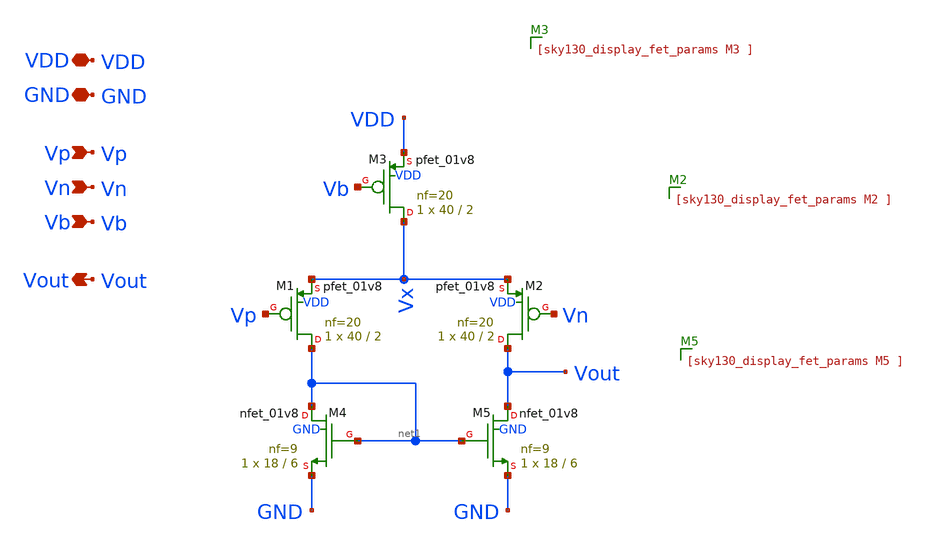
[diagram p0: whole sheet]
** sch_path: sch/archive/old/5t_ota_p.sch
**.subckt 5t_ota_p VDD Vp Vout GND Vn Vb
*.iopin VDD
*.ipin Vp
*.opin Vout
*.iopin GND
*.ipin Vn
*.ipin Vb
XM1 net1 Vp Vx VDD sky130_fd_pr__pfet_01v8 L=2 W=40 nf=20 ad='int((20 + 1)/2) * 40 / 20 * 0.29' as='int((20 + 2)/2) * 40 / 20 * 0.29'
+ pd='2*int((20 + 1)/2) * (40 / 20 + 0.29)' ps='2*int((20 + 2)/2) * (40 / 20 + 0.29)' nrd='0.29 / 40 '
+ nrs='0.29 / 40 ' sa=0 sb=0 sd=0 mult=1 m=1
XM2 Vout Vn Vx VDD sky130_fd_pr__pfet_01v8 L=2 W=40 nf=20 ad='int((20 + 1)/2) * 40 / 20 * 0.29' as='int((20 + 2)/2) * 40 / 20 * 0.29'
+ pd='2*int((20 + 1)/2) * (40 / 20 + 0.29)' ps='2*int((20 + 2)/2) * (40 / 20 + 0.29)' nrd='0.29 / 40 '
+ nrs='0.29 / 40 ' sa=0 sb=0 sd=0 mult=1 m=1
XM3 Vx Vb VDD VDD sky130_fd_pr__pfet_01v8 L=2 W=40 nf=20 ad='int((20 + 1)/2) * 40 / 20 * 0.29' as='int((20 + 2)/2) * 40 / 20 * 0.29'
+ pd='2*int((20 + 1)/2) * (40 / 20 + 0.29)' ps='2*int((20 + 2)/2) * (40 / 20 + 0.29)' nrd='0.29 / 40 '
+ nrs='0.29 / 40 ' sa=0 sb=0 sd=0 mult=1 m=1
XM4 net1 net1 GND GND sky130_fd_pr__nfet_01v8 L=6 W=18 nf=9 ad='int((9 + 1)/2) * 18 / 9 * 0.29' as='int((9 + 2)/2) * 18 / 9 * 0.29'
+ pd='2*int((9 + 1)/2) * (18 / 9 + 0.29)' ps='2*int((9 + 2)/2) * (18 / 9 + 0.29)' nrd='0.29 / 18 ' nrs='0.29 / 18 '
+ sa=0 sb=0 sd=0 mult=1 m=1
XM5 Vout net1 GND GND sky130_fd_pr__nfet_01v8 L=6 W=18 nf=9 ad='int((9 + 1)/2) * 18 / 9 * 0.29' as='int((9 + 2)/2) * 18 / 9 * 0.29'
+ pd='2*int((9 + 1)/2) * (18 / 9 + 0.29)' ps='2*int((9 + 2)/2) * (18 / 9 + 0.29)' nrd='0.29 / 18 ' nrs='0.29 / 18 '
+ sa=0 sb=0 sd=0 mult=1 m=1
**.ends
.end
